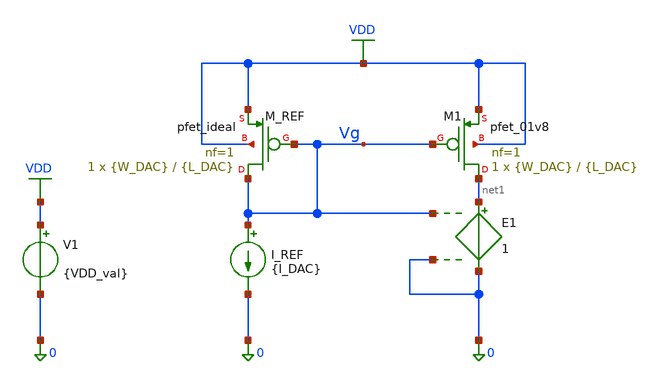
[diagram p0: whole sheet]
** sch_path: designs_backup/designs/lab2/lab2_mismatch.sch
**.subckt lab2_mismatch
I_REF Vg 0 {I_DAC}
E1 net1 0 Vg 0 1
V1 VDD 0 {VDD_val}
XM1 net1 Vg VDD VDD sky130_fd_pr__pfet_01v8 L={L_DAC} W={W_DAC} nf=1 ad='int((1 + 1)/2) * {W_DAC} / 1 * 0.29'
+ as='int((1 + 2)/2) * {W_DAC} / 1 * 0.29' pd='2*int((1 + 1)/2) * ({W_DAC} / 1 + 0.29)' ps='2*int((1 + 2)/2) * ({W_DAC} / 1 + 0.29)'
+ nrd='0.29 / {W_DAC} ' nrs='0.29 / {W_DAC} ' sa=0 sb=0 sd=0 mult=1 m=1
XM_REF Vg Vg VDD VDD sky130_fd_pr__pfet_ideal L={L_DAC} W={W_DAC} nf=1 ad='int((1 + 1)/2) * {W_DAC} / 1 * 0.29'
+ as='int((1 + 2)/2) * {W_DAC} / 1 * 0.29' pd='2*int((1 + 1)/2) * ({W_DAC} / 1 + 0.29)' ps='2*int((1 + 2)/2) * ({W_DAC} / 1 + 0.29)'
+ nrd='0.29 / {W_DAC} ' nrs='0.29 / {W_DAC} ' sa=0 sb=0 sd=0 mult=1 m=1
**** begin user architecture code

** opencircuitdesign pdks install
.lib $::SKYWATER_MODELS/sky130.lib.spice tt

* force include MC files
.include "$::SKYWATER_MODELS/parameters/montecarlo.spice"
.include "$::SKYWATER_MODELS/parameters/critical.spice"

* force mismatch/process params
.param mc_mm_switch = 1
.param mc_pr_switch = 0

* disable pfet_ideal from mismatch/process
.subckt sky130_fd_pr__pfet_ideal D G S B W=0.42 L=0.18  nf=1 ad='int((1 + 1)/2) * {W} / 1 * 0.29' as='int((1 + 2)/2) * {W} / 1 * 0.29'
+  pd='2*int((1 + 1)/2) * ({W} / 1 + 0.29)' ps='2*int((1 + 2)/2) * ({W} / 1 + 0.29)'   nrd='0.29 / {W}'
+ nrs='0.29 / {W}' sa=0 sb=0 sd=0 mult=1
  .param mc_mm_switch=0
  .param mc_pr_switch=0
  XIDEAL D G S B sky130_fd_pr__pfet_01v8 W={W} L={L}
  + nf={nf} ad={ad} as={as} pd={pd} ps={ps}
  + nrd={nrd} nrs={nrs} sa={sa} sb={sb} sd={sd} mult={mult}
.ends



.param W_DAC = 0.42 L_DAC = 0.18
.param I_DAC = 100n
.param VDD_val = 1.8
.options savecurrents

.control
  let runs = 100
  shell mkdir -p /foss/designs/lab2/results/1.8
  shell rm -f /foss/designs/lab2/results/1.8/M1_stats.dat
+ /foss/designs/lab2/results/1.8/M1_Iruns.dat

  foreach idac_val 100n 10u
    foreach case_idx 1 2 3
      if $case_idx = 1
        alterparam W_DAC = 0.42
        alterparam L_DAC = 0.18
      end
      if $case_idx = 2
        alterparam W_DAC = 5.0
        alterparam L_DAC = 2.0
      end
      if $case_idx = 3
        alterparam W_DAC = 2.0
        alterparam L_DAC = 5.0
      end
      alterparam I_DAC = $idac_val
      * allocate vector for currents
      let Ivec = vector(runs)
      let r = 0

      * reset and op to apply W/L changes
      reset
      op
      let W = @m.xm1.msky130_fd_pr__pfet_01v8[w] * 1e6
      let L = @m.xm1.msky130_fd_pr__pfet_01v8[l] * 1e6
      echo ----- W/L= $&W / $&L IDAC= $idac_val ----- >> /foss/designs/lab2/results/1.8/M1_Iruns.dat
      echo ----- W/L= $&W / $&L IDAC= $idac_val ----- >> /foss/designs/lab2/results/1.8/M1_stats.dat
      dowhile r < runs
        reset
        op
        let Ivec[r] = @m.xm1.msky130_fd_pr__pfet_01v8[id]
        let curI = Ivec[r] * 1e6
        set appendwrite
        echo RUN= $&r I[uA]= $&curI >> /foss/designs/lab2/results/1.8/M1_Iruns.dat
        let r = r + 1
        *break
      end

      * calculate stats
      let avgI = mean(Ivec) * 1e6
      let sigI = stddev(Ivec) * 1e6
      let ratio = sigI/avgI * 100
      * vecmin() would do the same as minimum() ; analogically is maximum() and vecmax()
      let minI = minimum(Ivec) * 1e6
      let maxI = maximum(Ivec) * 1e6

      echo MIN[uA]= $&minI MAX[uA]= $&maxI AVG[uA]= $&avgI SIGMA[uA]= $&sigI sigma/AVG[%]= $&ratio
+ >> /foss/designs/lab2/results/1.8/M1_stats.dat
      echo >> /foss/designs/lab2/results/1.8/M1_stats.dat
    end
  end
.endc


**** end user architecture code
**.ends
.GLOBAL VDD
.end
